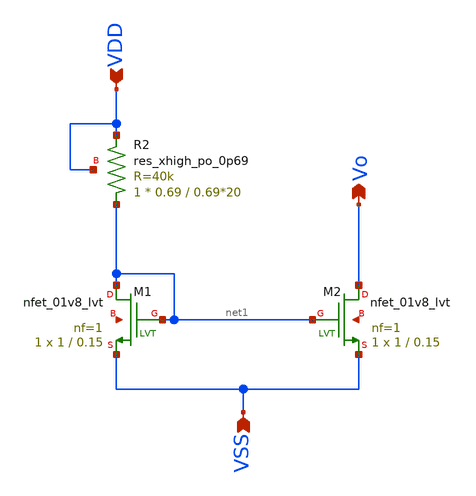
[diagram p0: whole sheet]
** sch_path: hw03/xschem/untitled.sch
**.subckt untitled VSS Vo VDD
*.ipin VSS
*.opin Vo
*.ipin VDD
XM1 net1 net1 VSS net2 sky130_fd_pr__nfet_01v8_lvt L=0.15 W=1 nf=1 ad='int((1 + 1)/2) * 1 / 1 * 0.29'
+ as='int((1 + 2)/2) * 1 / 1 * 0.29' pd='2*int((1 + 1)/2) * (1 / 1 + 0.29)' ps='2*int((1 + 2)/2) * (1 / 1 + 0.29)'
+ nrd='0.29 / 1 ' nrs='0.29 / 1 ' sa=0 sb=0 sd=0 mult=1 m=1
XM2 Vo net1 VSS net3 sky130_fd_pr__nfet_01v8_lvt L=0.15 W=1 nf=1 ad='int((1 + 1)/2) * 1 / 1 * 0.29' as='int((1 + 2)/2) * 1 / 1 * 0.29'
+ pd='2*int((1 + 1)/2) * (1 / 1 + 0.29)' ps='2*int((1 + 2)/2) * (1 / 1 + 0.29)' nrd='0.29 / 1 ' nrs='0.29 / 1 '
+ sa=0 sb=0 sd=0 mult=1 m=1
XR2 net1 VDD VDD sky130_fd_pr__res_xhigh_po_0p69 L=0.69*20 mult=1 m=1
**.ends
.end
